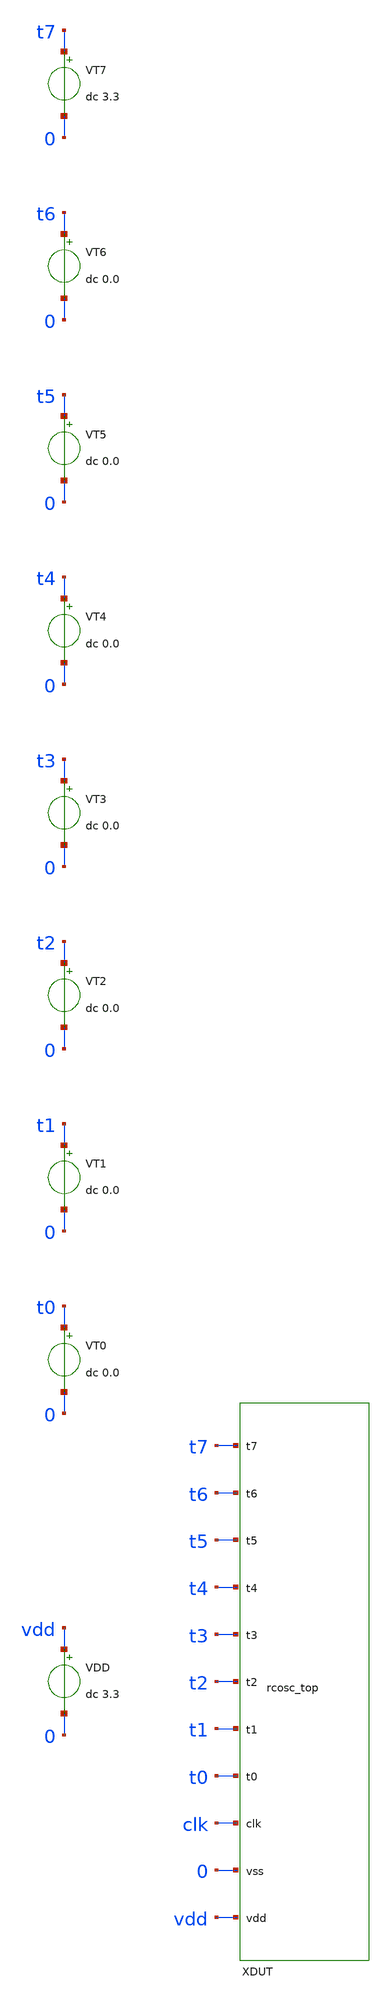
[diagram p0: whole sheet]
** sch_path: design/smoke_test.sch
**.subckt smoke_test
XXDUT vdd 0 clk t0 t1 t2 t3 t4 t5 t6 t7 rcosc_top
VDD vdd 0 dc 3.3
VT0 t0 0 dc 0.0
VT1 t1 0 dc 0.0
VT2 t2 0 dc 0.0
VT3 t3 0 dc 0.0
VT4 t4 0 dc 0.0
VT5 t5 0 dc 0.0
VT6 t6 0 dc 0.0
VT7 t7 0 dc 3.3
**** begin user architecture code


* pdk_include.spice is generated at run time by regen-netlist.sh /
* run-smoke-test.sh from $PDK_ROOT / $PDK, kept out of this schematic
* so it has no hardcoded, machine-specific path.
.include pdk_include.spice

.control
op
print v(vdd) v(vc) v(vh) v(vl) v(ibias) v(clk)
* Total DC current drawn from vdd at this .op point (issue #20): ngspice's
* passive sign convention on an independent source reports current flowing
* INTO its positive terminal, so i(vdd) is negative when the circuit is
* actually drawing current from the supply -- negate it to report a
* positive quiescent-current figure in microamps.
let iq_ua = -1e6*i(vdd)
print iq_ua
tran 200p 1200n
meas tran t_first_rise when v(clk)=1.65 rise=1
meas tran t_second_rise when v(clk)=1.65 rise=2
print t_first_rise t_second_rise
* Running quiescent current (issue #22). DR-0003 Row 4's target is stated
* as '< 500 uA (running)', and its anchor -- ST DS9826's IDDA(HSI48), 312
* uA typ -- is a datasheet supply-current figure for an oscillator that is
* oscillating. The .op figure above is NOT that quantity: a relaxation
* oscillator has no stable DC operating point, so the DC solve converges
* on the unstable equilibrium, which pins the charge-complete comparator
* XCMPH at its own output inverter's trip point -- holding that buffer,
* and the SR-latch NOR gate its mid-rail output drives, in full crowbar
* conduction, a state the running circuit occupies only in transit
* (measured: sim/iq/corners/). iq_run_ua below is the
* quantity Row 4 actually names: -i(vdd) averaged over 20 whole periods
* (rising edges 5..25, startup skipped). Both are printed, never one
* without the other -- see DR-0008.
let ivdd_ua = -1e6*i(vdd)
meas tran t_avg_start when v(clk)=1.65 rise=5
meas tran t_avg_end when v(clk)=1.65 rise=25
meas tran iq_run_ua AVG ivdd_ua FROM=$&t_avg_start TO=$&t_avg_end
quit
.endc


**** end user architecture code
**.ends

* expanding   symbol:  rcosc_top.sym # of pins=11
** sym_path: design/rcosc_top.sym
** sch_path: design/rcosc_top.sch
.subckt rcosc_top vdd vss clk t0 t1 t2 t3 t4 t5 t6 t7

*.iopin vdd
*.iopin vss
*.iopin clk
*.iopin t0
*.iopin t1
*.iopin t2
*.iopin t3
*.iopin t4
*.iopin t5
*.iopin t6
*.iopin t7
XXBIAS vdd vss vh vl ibias rcosc_bias
XXTRIM vdd vc vss t0 t1 t2 t3 t4 t5 t6 t7 vdd rcosc_trim_bank
XCTIMING vss vc cap_mim_1f0fF c_width=20u c_length=10u m=1
XXCMPH vdd vss ibias vc vh cmph_out rcosc_comparator
XXCMPL vdd vss ibias vl vc cmpl_out rcosc_comparator
XMDISCH vc clk vss vss nfet_03v3 L=0.5u W=20u nf=1 ad='int((nf+1)/2) * W/nf * 0.18u' as='int((nf+2)/2) * W/nf * 0.18u'
+ pd='2*int((nf+1)/2) * (W/nf + 0.18u)' ps='2*int((nf+2)/2) * (W/nf + 0.18u)' nrd='0.18u / W' nrs='0.18u / W'
+ sa=0 sb=0 sd=0 m=1
XMG1A qbar cmph_out vss vss nfet_03v3 L=0.5u W=2u nf=1 ad='int((nf+1)/2) * W/nf * 0.18u' as='int((nf+2)/2) * W/nf * 0.18u'
+ pd='2*int((nf+1)/2) * (W/nf + 0.18u)' ps='2*int((nf+2)/2) * (W/nf + 0.18u)' nrd='0.18u / W' nrs='0.18u / W'
+ sa=0 sb=0 sd=0 m=1
XMG1B qbar clk vss vss nfet_03v3 L=0.5u W=2u nf=1 ad='int((nf+1)/2) * W/nf * 0.18u' as='int((nf+2)/2) * W/nf * 0.18u'
+ pd='2*int((nf+1)/2) * (W/nf + 0.18u)' ps='2*int((nf+2)/2) * (W/nf + 0.18u)' nrd='0.18u / W' nrs='0.18u / W'
+ sa=0 sb=0 sd=0 m=1
XMG1C mid1 cmph_out vdd vdd pfet_03v3 L=0.5u W=4u nf=1 ad='int((nf+1)/2) * W/nf * 0.18u' as='int((nf+2)/2) * W/nf * 0.18u'
+ pd='2*int((nf+1)/2) * (W/nf + 0.18u)' ps='2*int((nf+2)/2) * (W/nf + 0.18u)' nrd='0.18u / W' nrs='0.18u / W'
+ sa=0 sb=0 sd=0 m=1
XMG1D qbar clk mid1 vdd pfet_03v3 L=0.5u W=4u nf=1 ad='int((nf+1)/2) * W/nf * 0.18u' as='int((nf+2)/2) * W/nf * 0.18u'
+ pd='2*int((nf+1)/2) * (W/nf + 0.18u)' ps='2*int((nf+2)/2) * (W/nf + 0.18u)' nrd='0.18u / W' nrs='0.18u / W'
+ sa=0 sb=0 sd=0 m=1
XMG2A clk cmpl_out vss vss nfet_03v3 L=0.5u W=2u nf=1 ad='int((nf+1)/2) * W/nf * 0.18u' as='int((nf+2)/2) * W/nf * 0.18u'
+ pd='2*int((nf+1)/2) * (W/nf + 0.18u)' ps='2*int((nf+2)/2) * (W/nf + 0.18u)' nrd='0.18u / W' nrs='0.18u / W'
+ sa=0 sb=0 sd=0 m=1
XMG2B clk qbar vss vss nfet_03v3 L=0.5u W=2u nf=1 ad='int((nf+1)/2) * W/nf * 0.18u' as='int((nf+2)/2) * W/nf * 0.18u'
+ pd='2*int((nf+1)/2) * (W/nf + 0.18u)' ps='2*int((nf+2)/2) * (W/nf + 0.18u)' nrd='0.18u / W' nrs='0.18u / W'
+ sa=0 sb=0 sd=0 m=1
XMG2C mid2 cmpl_out vdd vdd pfet_03v3 L=0.5u W=4u nf=1 ad='int((nf+1)/2) * W/nf * 0.18u' as='int((nf+2)/2) * W/nf * 0.18u'
+ pd='2*int((nf+1)/2) * (W/nf + 0.18u)' ps='2*int((nf+2)/2) * (W/nf + 0.18u)' nrd='0.18u / W' nrs='0.18u / W'
+ sa=0 sb=0 sd=0 m=1
XMG2D clk qbar mid2 vdd pfet_03v3 L=0.5u W=4u nf=1 ad='int((nf+1)/2) * W/nf * 0.18u' as='int((nf+2)/2) * W/nf * 0.18u'
+ pd='2*int((nf+1)/2) * (W/nf + 0.18u)' ps='2*int((nf+2)/2) * (W/nf + 0.18u)' nrd='0.18u / W' nrs='0.18u / W'
+ sa=0 sb=0 sd=0 m=1
.ends


* expanding   symbol:  rcosc_bias.sym # of pins=5
** sym_path: design/rcosc_bias.sym
** sch_path: design/rcosc_bias.sch
.subckt rcosc_bias vdd vss vh vl ibias

*.iopin vdd
*.iopin vss
*.iopin vh
*.iopin vl
*.iopin ibias
XRBA vdd vh vss ppolyf_u_1k r_width=2u r_length=100u m=1
XRBB vh vl vss ppolyf_u_1k r_width=2u r_length=100u m=1
XRBC vl vss vss ppolyf_u_1k r_width=2u r_length=100u m=1
XN1 ibias ibias vss vss nfet_03v3 L=1u W=2u nf=1 ad='int((nf+1)/2) * W/nf * 0.18u' as='int((nf+2)/2) * W/nf * 0.18u'
+ pd='2*int((nf+1)/2) * (W/nf + 0.18u)' ps='2*int((nf+2)/2) * (W/nf + 0.18u)' nrd='0.18u / W' nrs='0.18u / W'
+ sa=0 sb=0 sd=0 m=1
XN2 pb ibias n2s vss nfet_03v3 L=1u W=16u nf=8 ad='int((nf+1)/2) * W/nf * 0.18u' as='int((nf+2)/2) * W/nf * 0.18u'
+ pd='2*int((nf+1)/2) * (W/nf + 0.18u)' ps='2*int((nf+2)/2) * (W/nf + 0.18u)' nrd='0.18u / W' nrs='0.18u / W'
+ sa=0 sb=0 sd=0 m=1
XRZ n2s vss vss ppolyf_u_1k r_width=2u r_length=24u m=1
XP1 pb pb vdd vdd pfet_03v3 L=1u W=4u nf=1 ad='int((nf+1)/2) * W/nf * 0.18u' as='int((nf+2)/2) * W/nf * 0.18u'
+ pd='2*int((nf+1)/2) * (W/nf + 0.18u)' ps='2*int((nf+2)/2) * (W/nf + 0.18u)' nrd='0.18u / W' nrs='0.18u / W'
+ sa=0 sb=0 sd=0 m=1
XP2 ibias pb vdd vdd pfet_03v3 L=1u W=4u nf=1 ad='int((nf+1)/2) * W/nf * 0.18u' as='int((nf+2)/2) * W/nf * 0.18u'
+ pd='2*int((nf+1)/2) * (W/nf + 0.18u)' ps='2*int((nf+2)/2) * (W/nf + 0.18u)' nrd='0.18u / W' nrs='0.18u / W'
+ sa=0 sb=0 sd=0 m=1
XSEED vdd ibias vss ppolyf_u_1k r_width=2u r_length=4860u m=1
.ends


* expanding   symbol:  rcosc_trim_bank.sym # of pins=12
** sym_path: design/rcosc_trim_bank.sym
** sch_path: design/rcosc_trim_bank.sch
.subckt rcosc_trim_bank p m vss t0 t1 t2 t3 t4 t5 t6 t7 vdd

*.iopin p
*.iopin m
*.iopin vss
*.iopin t0
*.iopin t1
*.iopin t2
*.iopin t3
*.iopin t4
*.iopin t5
*.iopin t6
*.iopin t7
*.iopin vdd
XRFIX p c1 vss ppolyf_u_1k r_width=2u r_length=17.198u m=1
XR0 c1 c2 vss ppolyf_u_1k r_width=2u r_length=0.7482u m=1
XSW0 c1 t0 c2 vss nfet_03v3 L=0.28u W=24uu nf=1 ad='int((nf+1)/2) * W/nf * 0.18u' as='int((nf+2)/2) * W/nf * 0.18u'
+ pd='2*int((nf+1)/2) * (W/nf + 0.18u)' ps='2*int((nf+2)/2) * (W/nf + 0.18u)' nrd='0.18u / W' nrs='0.18u / W'
+ sa=0 sb=0 sd=0 m=1
XPW0 c2 tb0 c1 vdd pfet_03v3 L=0.28u W=24uu nf=1 ad='int((nf+1)/2) * W/nf * 0.18u' as='int((nf+2)/2) * W/nf * 0.18u'
+ pd='2*int((nf+1)/2) * (W/nf + 0.18u)' ps='2*int((nf+2)/2) * (W/nf + 0.18u)' nrd='0.18u / W' nrs='0.18u / W'
+ sa=0 sb=0 sd=0 m=1
XNINV0 tb0 t0 vss vss nfet_03v3 L=0.5u W=2u nf=1 ad='int((nf+1)/2) * W/nf * 0.18u' as='int((nf+2)/2) * W/nf * 0.18u'
+ pd='2*int((nf+1)/2) * (W/nf + 0.18u)' ps='2*int((nf+2)/2) * (W/nf + 0.18u)' nrd='0.18u / W' nrs='0.18u / W'
+ sa=0 sb=0 sd=0 m=1
XPINV0 tb0 t0 vdd vdd pfet_03v3 L=0.5u W=4u nf=1 ad='int((nf+1)/2) * W/nf * 0.18u' as='int((nf+2)/2) * W/nf * 0.18u'
+ pd='2*int((nf+1)/2) * (W/nf + 0.18u)' ps='2*int((nf+2)/2) * (W/nf + 0.18u)' nrd='0.18u / W' nrs='0.18u / W'
+ sa=0 sb=0 sd=0 m=1
XR1 c2 c3 vss ppolyf_u_1k r_width=2u r_length=1.4965u m=1
XSW1 c2 t1 c3 vss nfet_03v3 L=0.28u W=16uu nf=1 ad='int((nf+1)/2) * W/nf * 0.18u' as='int((nf+2)/2) * W/nf * 0.18u'
+ pd='2*int((nf+1)/2) * (W/nf + 0.18u)' ps='2*int((nf+2)/2) * (W/nf + 0.18u)' nrd='0.18u / W' nrs='0.18u / W'
+ sa=0 sb=0 sd=0 m=1
XPW1 c3 tb1 c2 vdd pfet_03v3 L=0.28u W=16uu nf=1 ad='int((nf+1)/2) * W/nf * 0.18u' as='int((nf+2)/2) * W/nf * 0.18u'
+ pd='2*int((nf+1)/2) * (W/nf + 0.18u)' ps='2*int((nf+2)/2) * (W/nf + 0.18u)' nrd='0.18u / W' nrs='0.18u / W'
+ sa=0 sb=0 sd=0 m=1
XNINV1 tb1 t1 vss vss nfet_03v3 L=0.5u W=2u nf=1 ad='int((nf+1)/2) * W/nf * 0.18u' as='int((nf+2)/2) * W/nf * 0.18u'
+ pd='2*int((nf+1)/2) * (W/nf + 0.18u)' ps='2*int((nf+2)/2) * (W/nf + 0.18u)' nrd='0.18u / W' nrs='0.18u / W'
+ sa=0 sb=0 sd=0 m=1
XPINV1 tb1 t1 vdd vdd pfet_03v3 L=0.5u W=4u nf=1 ad='int((nf+1)/2) * W/nf * 0.18u' as='int((nf+2)/2) * W/nf * 0.18u'
+ pd='2*int((nf+1)/2) * (W/nf + 0.18u)' ps='2*int((nf+2)/2) * (W/nf + 0.18u)' nrd='0.18u / W' nrs='0.18u / W'
+ sa=0 sb=0 sd=0 m=1
XR2 c3 c4 vss ppolyf_u_1k r_width=2u r_length=2.993u m=1
XSW2 c3 t2 c4 vss nfet_03v3 L=0.28u W=12uu nf=1 ad='int((nf+1)/2) * W/nf * 0.18u' as='int((nf+2)/2) * W/nf * 0.18u'
+ pd='2*int((nf+1)/2) * (W/nf + 0.18u)' ps='2*int((nf+2)/2) * (W/nf + 0.18u)' nrd='0.18u / W' nrs='0.18u / W'
+ sa=0 sb=0 sd=0 m=1
XPW2 c4 tb2 c3 vdd pfet_03v3 L=0.28u W=12uu nf=1 ad='int((nf+1)/2) * W/nf * 0.18u' as='int((nf+2)/2) * W/nf * 0.18u'
+ pd='2*int((nf+1)/2) * (W/nf + 0.18u)' ps='2*int((nf+2)/2) * (W/nf + 0.18u)' nrd='0.18u / W' nrs='0.18u / W'
+ sa=0 sb=0 sd=0 m=1
XNINV2 tb2 t2 vss vss nfet_03v3 L=0.5u W=2u nf=1 ad='int((nf+1)/2) * W/nf * 0.18u' as='int((nf+2)/2) * W/nf * 0.18u'
+ pd='2*int((nf+1)/2) * (W/nf + 0.18u)' ps='2*int((nf+2)/2) * (W/nf + 0.18u)' nrd='0.18u / W' nrs='0.18u / W'
+ sa=0 sb=0 sd=0 m=1
XPINV2 tb2 t2 vdd vdd pfet_03v3 L=0.5u W=4u nf=1 ad='int((nf+1)/2) * W/nf * 0.18u' as='int((nf+2)/2) * W/nf * 0.18u'
+ pd='2*int((nf+1)/2) * (W/nf + 0.18u)' ps='2*int((nf+2)/2) * (W/nf + 0.18u)' nrd='0.18u / W' nrs='0.18u / W'
+ sa=0 sb=0 sd=0 m=1
XR3 c4 c5 vss ppolyf_u_1k r_width=2u r_length=5.9859u m=1
XSW3 c4 t3 c5 vss nfet_03v3 L=0.28u W=8uu nf=1 ad='int((nf+1)/2) * W/nf * 0.18u' as='int((nf+2)/2) * W/nf * 0.18u'
+ pd='2*int((nf+1)/2) * (W/nf + 0.18u)' ps='2*int((nf+2)/2) * (W/nf + 0.18u)' nrd='0.18u / W' nrs='0.18u / W'
+ sa=0 sb=0 sd=0 m=1
XPW3 c5 tb3 c4 vdd pfet_03v3 L=0.28u W=8uu nf=1 ad='int((nf+1)/2) * W/nf * 0.18u' as='int((nf+2)/2) * W/nf * 0.18u'
+ pd='2*int((nf+1)/2) * (W/nf + 0.18u)' ps='2*int((nf+2)/2) * (W/nf + 0.18u)' nrd='0.18u / W' nrs='0.18u / W'
+ sa=0 sb=0 sd=0 m=1
XNINV3 tb3 t3 vss vss nfet_03v3 L=0.5u W=2u nf=1 ad='int((nf+1)/2) * W/nf * 0.18u' as='int((nf+2)/2) * W/nf * 0.18u'
+ pd='2*int((nf+1)/2) * (W/nf + 0.18u)' ps='2*int((nf+2)/2) * (W/nf + 0.18u)' nrd='0.18u / W' nrs='0.18u / W'
+ sa=0 sb=0 sd=0 m=1
XPINV3 tb3 t3 vdd vdd pfet_03v3 L=0.5u W=4u nf=1 ad='int((nf+1)/2) * W/nf * 0.18u' as='int((nf+2)/2) * W/nf * 0.18u'
+ pd='2*int((nf+1)/2) * (W/nf + 0.18u)' ps='2*int((nf+2)/2) * (W/nf + 0.18u)' nrd='0.18u / W' nrs='0.18u / W'
+ sa=0 sb=0 sd=0 m=1
XR4 c5 c6 vss ppolyf_u_1k r_width=2u r_length=11.9719u m=1
XSW4 c5 t4 c6 vss nfet_03v3 L=0.28u W=6uu nf=1 ad='int((nf+1)/2) * W/nf * 0.18u' as='int((nf+2)/2) * W/nf * 0.18u'
+ pd='2*int((nf+1)/2) * (W/nf + 0.18u)' ps='2*int((nf+2)/2) * (W/nf + 0.18u)' nrd='0.18u / W' nrs='0.18u / W'
+ sa=0 sb=0 sd=0 m=1
XPW4 c6 tb4 c5 vdd pfet_03v3 L=0.28u W=6uu nf=1 ad='int((nf+1)/2) * W/nf * 0.18u' as='int((nf+2)/2) * W/nf * 0.18u'
+ pd='2*int((nf+1)/2) * (W/nf + 0.18u)' ps='2*int((nf+2)/2) * (W/nf + 0.18u)' nrd='0.18u / W' nrs='0.18u / W'
+ sa=0 sb=0 sd=0 m=1
XNINV4 tb4 t4 vss vss nfet_03v3 L=0.5u W=2u nf=1 ad='int((nf+1)/2) * W/nf * 0.18u' as='int((nf+2)/2) * W/nf * 0.18u'
+ pd='2*int((nf+1)/2) * (W/nf + 0.18u)' ps='2*int((nf+2)/2) * (W/nf + 0.18u)' nrd='0.18u / W' nrs='0.18u / W'
+ sa=0 sb=0 sd=0 m=1
XPINV4 tb4 t4 vdd vdd pfet_03v3 L=0.5u W=4u nf=1 ad='int((nf+1)/2) * W/nf * 0.18u' as='int((nf+2)/2) * W/nf * 0.18u'
+ pd='2*int((nf+1)/2) * (W/nf + 0.18u)' ps='2*int((nf+2)/2) * (W/nf + 0.18u)' nrd='0.18u / W' nrs='0.18u / W'
+ sa=0 sb=0 sd=0 m=1
XR5 c6 c7 vss ppolyf_u_1k r_width=2u r_length=23.9438u m=1
XSW5 c6 t5 c7 vss nfet_03v3 L=0.28u W=5uu nf=1 ad='int((nf+1)/2) * W/nf * 0.18u' as='int((nf+2)/2) * W/nf * 0.18u'
+ pd='2*int((nf+1)/2) * (W/nf + 0.18u)' ps='2*int((nf+2)/2) * (W/nf + 0.18u)' nrd='0.18u / W' nrs='0.18u / W'
+ sa=0 sb=0 sd=0 m=1
XPW5 c7 tb5 c6 vdd pfet_03v3 L=0.28u W=5uu nf=1 ad='int((nf+1)/2) * W/nf * 0.18u' as='int((nf+2)/2) * W/nf * 0.18u'
+ pd='2*int((nf+1)/2) * (W/nf + 0.18u)' ps='2*int((nf+2)/2) * (W/nf + 0.18u)' nrd='0.18u / W' nrs='0.18u / W'
+ sa=0 sb=0 sd=0 m=1
XNINV5 tb5 t5 vss vss nfet_03v3 L=0.5u W=2u nf=1 ad='int((nf+1)/2) * W/nf * 0.18u' as='int((nf+2)/2) * W/nf * 0.18u'
+ pd='2*int((nf+1)/2) * (W/nf + 0.18u)' ps='2*int((nf+2)/2) * (W/nf + 0.18u)' nrd='0.18u / W' nrs='0.18u / W'
+ sa=0 sb=0 sd=0 m=1
XPINV5 tb5 t5 vdd vdd pfet_03v3 L=0.5u W=4u nf=1 ad='int((nf+1)/2) * W/nf * 0.18u' as='int((nf+2)/2) * W/nf * 0.18u'
+ pd='2*int((nf+1)/2) * (W/nf + 0.18u)' ps='2*int((nf+2)/2) * (W/nf + 0.18u)' nrd='0.18u / W' nrs='0.18u / W'
+ sa=0 sb=0 sd=0 m=1
XR6 c7 c8 vss ppolyf_u_1k r_width=2u r_length=47.8876u m=1
XSW6 c7 t6 c8 vss nfet_03v3 L=0.28u W=4uu nf=1 ad='int((nf+1)/2) * W/nf * 0.18u' as='int((nf+2)/2) * W/nf * 0.18u'
+ pd='2*int((nf+1)/2) * (W/nf + 0.18u)' ps='2*int((nf+2)/2) * (W/nf + 0.18u)' nrd='0.18u / W' nrs='0.18u / W'
+ sa=0 sb=0 sd=0 m=1
XPW6 c8 tb6 c7 vdd pfet_03v3 L=0.28u W=4uu nf=1 ad='int((nf+1)/2) * W/nf * 0.18u' as='int((nf+2)/2) * W/nf * 0.18u'
+ pd='2*int((nf+1)/2) * (W/nf + 0.18u)' ps='2*int((nf+2)/2) * (W/nf + 0.18u)' nrd='0.18u / W' nrs='0.18u / W'
+ sa=0 sb=0 sd=0 m=1
XNINV6 tb6 t6 vss vss nfet_03v3 L=0.5u W=2u nf=1 ad='int((nf+1)/2) * W/nf * 0.18u' as='int((nf+2)/2) * W/nf * 0.18u'
+ pd='2*int((nf+1)/2) * (W/nf + 0.18u)' ps='2*int((nf+2)/2) * (W/nf + 0.18u)' nrd='0.18u / W' nrs='0.18u / W'
+ sa=0 sb=0 sd=0 m=1
XPINV6 tb6 t6 vdd vdd pfet_03v3 L=0.5u W=4u nf=1 ad='int((nf+1)/2) * W/nf * 0.18u' as='int((nf+2)/2) * W/nf * 0.18u'
+ pd='2*int((nf+1)/2) * (W/nf + 0.18u)' ps='2*int((nf+2)/2) * (W/nf + 0.18u)' nrd='0.18u / W' nrs='0.18u / W'
+ sa=0 sb=0 sd=0 m=1
XR7 c8 m vss ppolyf_u_1k r_width=2u r_length=95.7751u m=1
XSW7 c8 t7 m vss nfet_03v3 L=0.28u W=3uu nf=1 ad='int((nf+1)/2) * W/nf * 0.18u' as='int((nf+2)/2) * W/nf * 0.18u'
+ pd='2*int((nf+1)/2) * (W/nf + 0.18u)' ps='2*int((nf+2)/2) * (W/nf + 0.18u)' nrd='0.18u / W' nrs='0.18u / W'
+ sa=0 sb=0 sd=0 m=1
XPW7 m tb7 c8 vdd pfet_03v3 L=0.28u W=3uu nf=1 ad='int((nf+1)/2) * W/nf * 0.18u' as='int((nf+2)/2) * W/nf * 0.18u'
+ pd='2*int((nf+1)/2) * (W/nf + 0.18u)' ps='2*int((nf+2)/2) * (W/nf + 0.18u)' nrd='0.18u / W' nrs='0.18u / W'
+ sa=0 sb=0 sd=0 m=1
XNINV7 tb7 t7 vss vss nfet_03v3 L=0.5u W=2u nf=1 ad='int((nf+1)/2) * W/nf * 0.18u' as='int((nf+2)/2) * W/nf * 0.18u'
+ pd='2*int((nf+1)/2) * (W/nf + 0.18u)' ps='2*int((nf+2)/2) * (W/nf + 0.18u)' nrd='0.18u / W' nrs='0.18u / W'
+ sa=0 sb=0 sd=0 m=1
XPINV7 tb7 t7 vdd vdd pfet_03v3 L=0.5u W=4u nf=1 ad='int((nf+1)/2) * W/nf * 0.18u' as='int((nf+2)/2) * W/nf * 0.18u'
+ pd='2*int((nf+1)/2) * (W/nf + 0.18u)' ps='2*int((nf+2)/2) * (W/nf + 0.18u)' nrd='0.18u / W' nrs='0.18u / W'
+ sa=0 sb=0 sd=0 m=1
.ends


* expanding   symbol:  rcosc_comparator.sym # of pins=6
** sym_path: design/rcosc_comparator.sym
** sch_path: design/rcosc_comparator.sch
.subckt rcosc_comparator vdd vss ibias inp inn out

*.iopin vdd
*.iopin vss
*.iopin ibias
*.iopin inp
*.iopin inn
*.iopin out
XMTAIL tail ibias vss vss nfet_03v3 L=1u W=16u nf=8 ad='int((nf+1)/2) * W/nf * 0.18u' as='int((nf+2)/2) * W/nf * 0.18u'
+ pd='2*int((nf+1)/2) * (W/nf + 0.18u)' ps='2*int((nf+2)/2) * (W/nf + 0.18u)' nrd='0.18u / W' nrs='0.18u / W'
+ sa=0 sb=0 sd=0 m=1
XMINP dp inp tail vss nfet_03v3 L=0.5u W=4u nf=1 ad='int((nf+1)/2) * W/nf * 0.18u' as='int((nf+2)/2) * W/nf * 0.18u'
+ pd='2*int((nf+1)/2) * (W/nf + 0.18u)' ps='2*int((nf+2)/2) * (W/nf + 0.18u)' nrd='0.18u / W' nrs='0.18u / W'
+ sa=0 sb=0 sd=0 m=1
XMINN dn inn tail vss nfet_03v3 L=0.5u W=4u nf=1 ad='int((nf+1)/2) * W/nf * 0.18u' as='int((nf+2)/2) * W/nf * 0.18u'
+ pd='2*int((nf+1)/2) * (W/nf + 0.18u)' ps='2*int((nf+2)/2) * (W/nf + 0.18u)' nrd='0.18u / W' nrs='0.18u / W'
+ sa=0 sb=0 sd=0 m=1
XMLOADA dn dn vdd vdd pfet_03v3 L=1u W=4u nf=1 ad='int((nf+1)/2) * W/nf * 0.18u' as='int((nf+2)/2) * W/nf * 0.18u'
+ pd='2*int((nf+1)/2) * (W/nf + 0.18u)' ps='2*int((nf+2)/2) * (W/nf + 0.18u)' nrd='0.18u / W' nrs='0.18u / W'
+ sa=0 sb=0 sd=0 m=1
XMLOADB dp dn vdd vdd pfet_03v3 L=1u W=4u nf=1 ad='int((nf+1)/2) * W/nf * 0.18u' as='int((nf+2)/2) * W/nf * 0.18u'
+ pd='2*int((nf+1)/2) * (W/nf + 0.18u)' ps='2*int((nf+2)/2) * (W/nf + 0.18u)' nrd='0.18u / W' nrs='0.18u / W'
+ sa=0 sb=0 sd=0 m=1
XMBUFP out dp vdd vdd pfet_03v3 L=0.5u W=4u nf=1 ad='int((nf+1)/2) * W/nf * 0.18u' as='int((nf+2)/2) * W/nf * 0.18u'
+ pd='2*int((nf+1)/2) * (W/nf + 0.18u)' ps='2*int((nf+2)/2) * (W/nf + 0.18u)' nrd='0.18u / W' nrs='0.18u / W'
+ sa=0 sb=0 sd=0 m=1
XMBUFN out dp vss vss nfet_03v3 L=0.5u W=1u nf=1 ad='int((nf+1)/2) * W/nf * 0.18u' as='int((nf+2)/2) * W/nf * 0.18u'
+ pd='2*int((nf+1)/2) * (W/nf + 0.18u)' ps='2*int((nf+2)/2) * (W/nf + 0.18u)' nrd='0.18u / W' nrs='0.18u / W'
+ sa=0 sb=0 sd=0 m=1
.ends

.end
